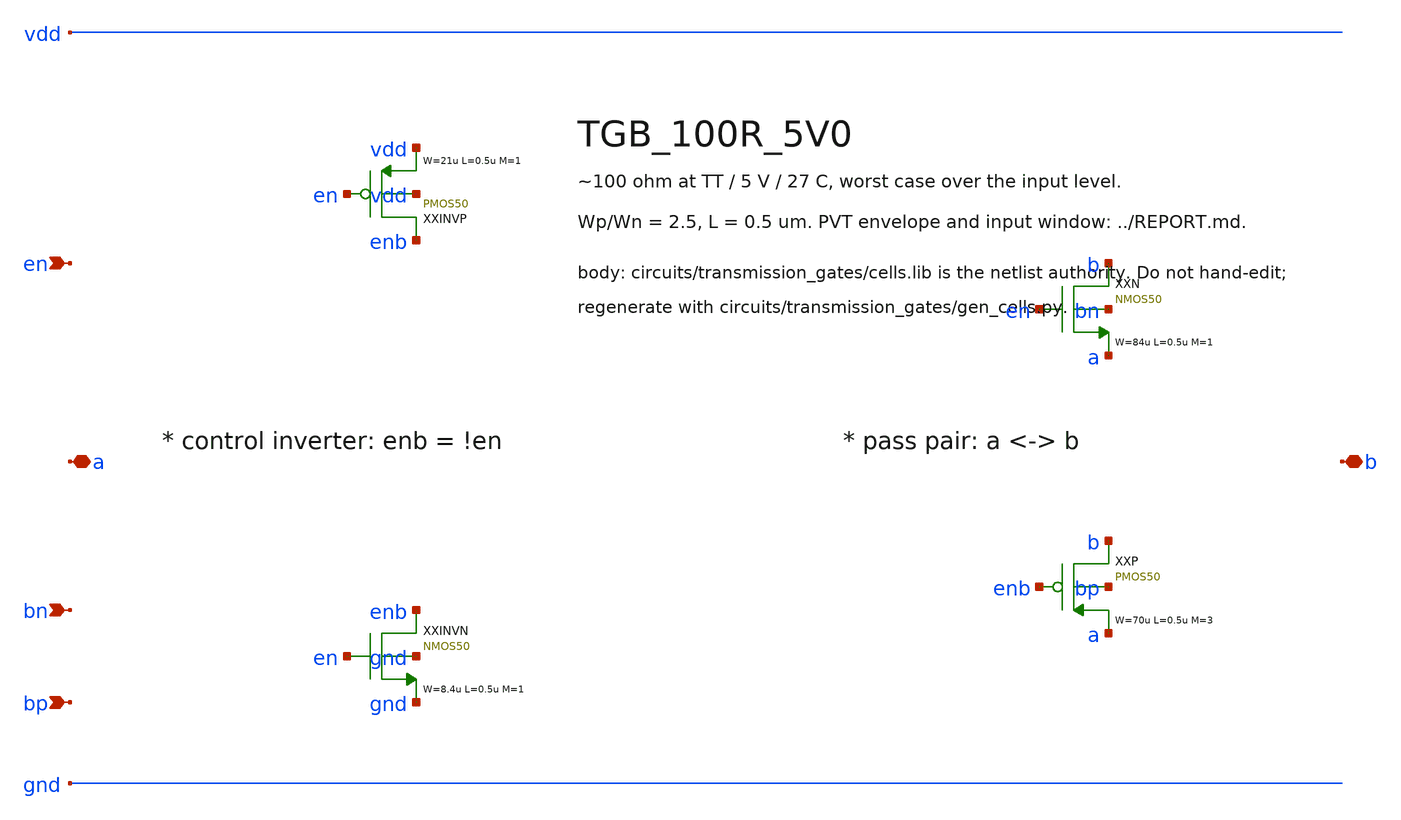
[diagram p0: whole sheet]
** sch_path: xschem/transmission_gates/TGB_100R_5V0.sch
**.subckt TGB_100R_5V0 a b en bn bp
*.iopin a
*.iopin b
*.ipin en
*.ipin bn
*.ipin bp
XXINVP enb en vdd vdd PMOS50 W=21u L=0.5u M=1 MM_SIGMA=0
XXINVN enb en gnd gnd NMOS50 W=8.4u L=0.5u M=1 MM_SIGMA=0
XXN b en a bn NMOS50 W=84u L=0.5u M=1 MM_SIGMA=0
XXP b enb a bp PMOS50 W=70u L=0.5u M=3 MM_SIGMA=0
**.ends
.end
